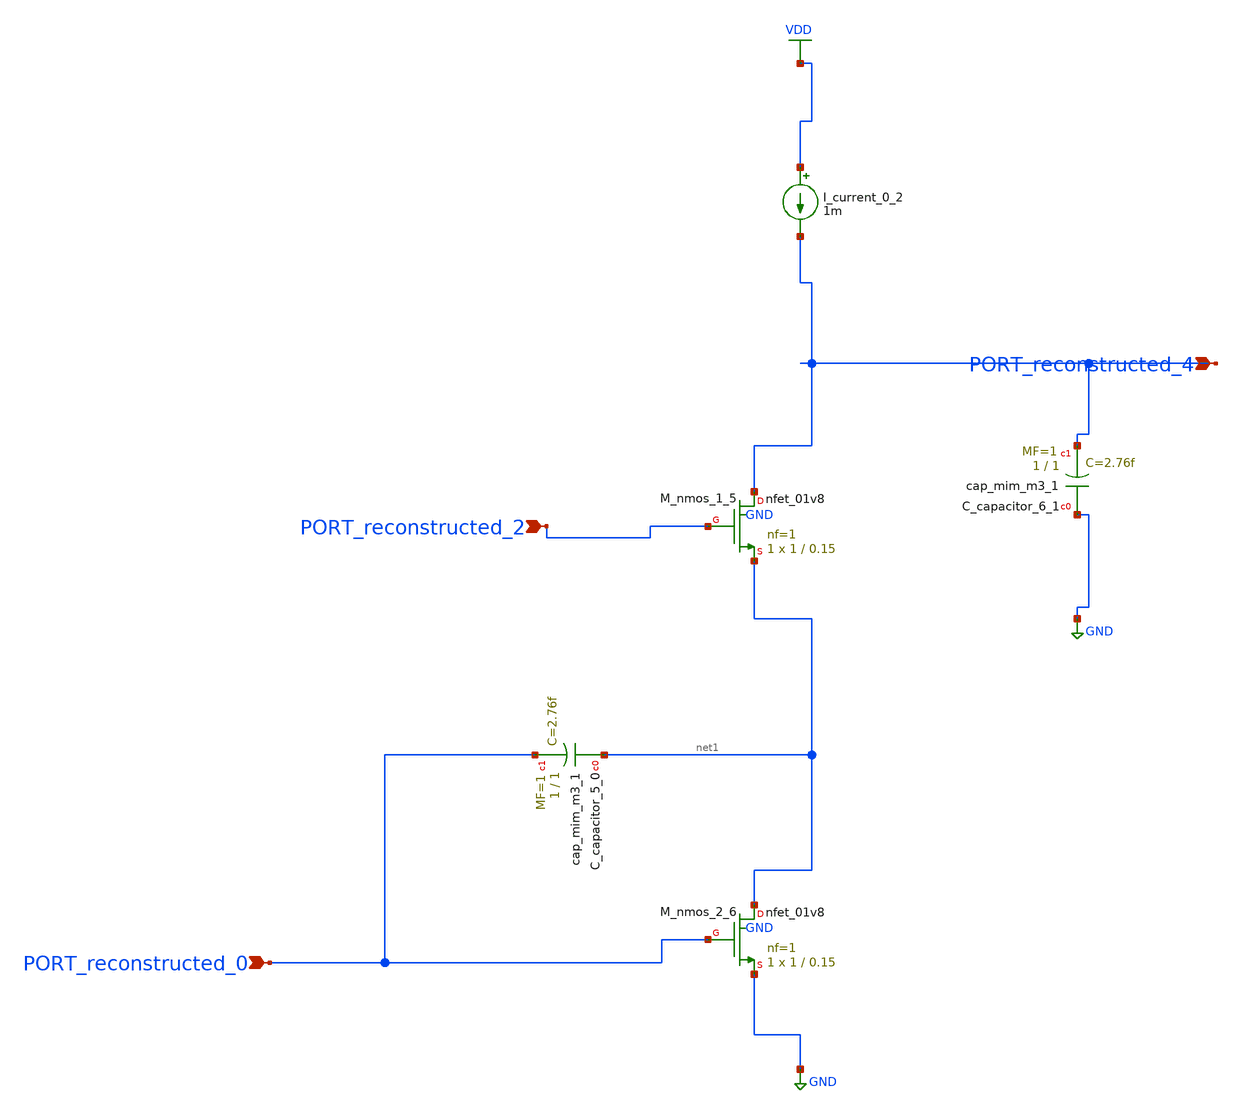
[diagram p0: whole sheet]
** sch_path: schematics/AMSNet/423.sch
**.subckt 423 PORT_reconstructed_2 PORT_reconstructed_4 PORT_reconstructed_0
*.ipin PORT_reconstructed_2
*.ipin PORT_reconstructed_4
*.ipin PORT_reconstructed_0
XC_capacitor_5_0 net1 PORT_reconstructed_0 sky130_fd_pr__cap_mim_m3_1 W=1 L=1 MF=1 m=1
XC_capacitor_6_1 GND PORT_reconstructed_4 sky130_fd_pr__cap_mim_m3_1 W=1 L=1 MF=1 m=1
I_current_0_2 VDD PORT_reconstructed_4 1m
XM_nmos_1_5 PORT_reconstructed_4 PORT_reconstructed_2 net1 GND sky130_fd_pr__nfet_01v8 L=0.15 W=1 nf=1
+ ad='int((1 + 1)/2) * 1 / 1 * 0.29' as='int((1 + 2)/2) * 1 / 1 * 0.29' pd='2*int((1 + 1)/2) * (1 / 1 + 0.29)'
+ ps='2*int((1 + 2)/2) * (1 / 1 + 0.29)' nrd='0.29 / 1 ' nrs='0.29 / 1 ' sa=0 sb=0 sd=0 mult=1 m=1
XM_nmos_2_6 net1 PORT_reconstructed_0 GND GND sky130_fd_pr__nfet_01v8 L=0.15 W=1 nf=1 ad='int((1 + 1)/2) * 1 / 1 * 0.29'
+ as='int((1 + 2)/2) * 1 / 1 * 0.29' pd='2*int((1 + 1)/2) * (1 / 1 + 0.29)' ps='2*int((1 + 2)/2) * (1 / 1 + 0.29)'
+ nrd='0.29 / 1 ' nrs='0.29 / 1 ' sa=0 sb=0 sd=0 mult=1 m=1
**.ends
.GLOBAL GND
.GLOBAL VDD
.end
